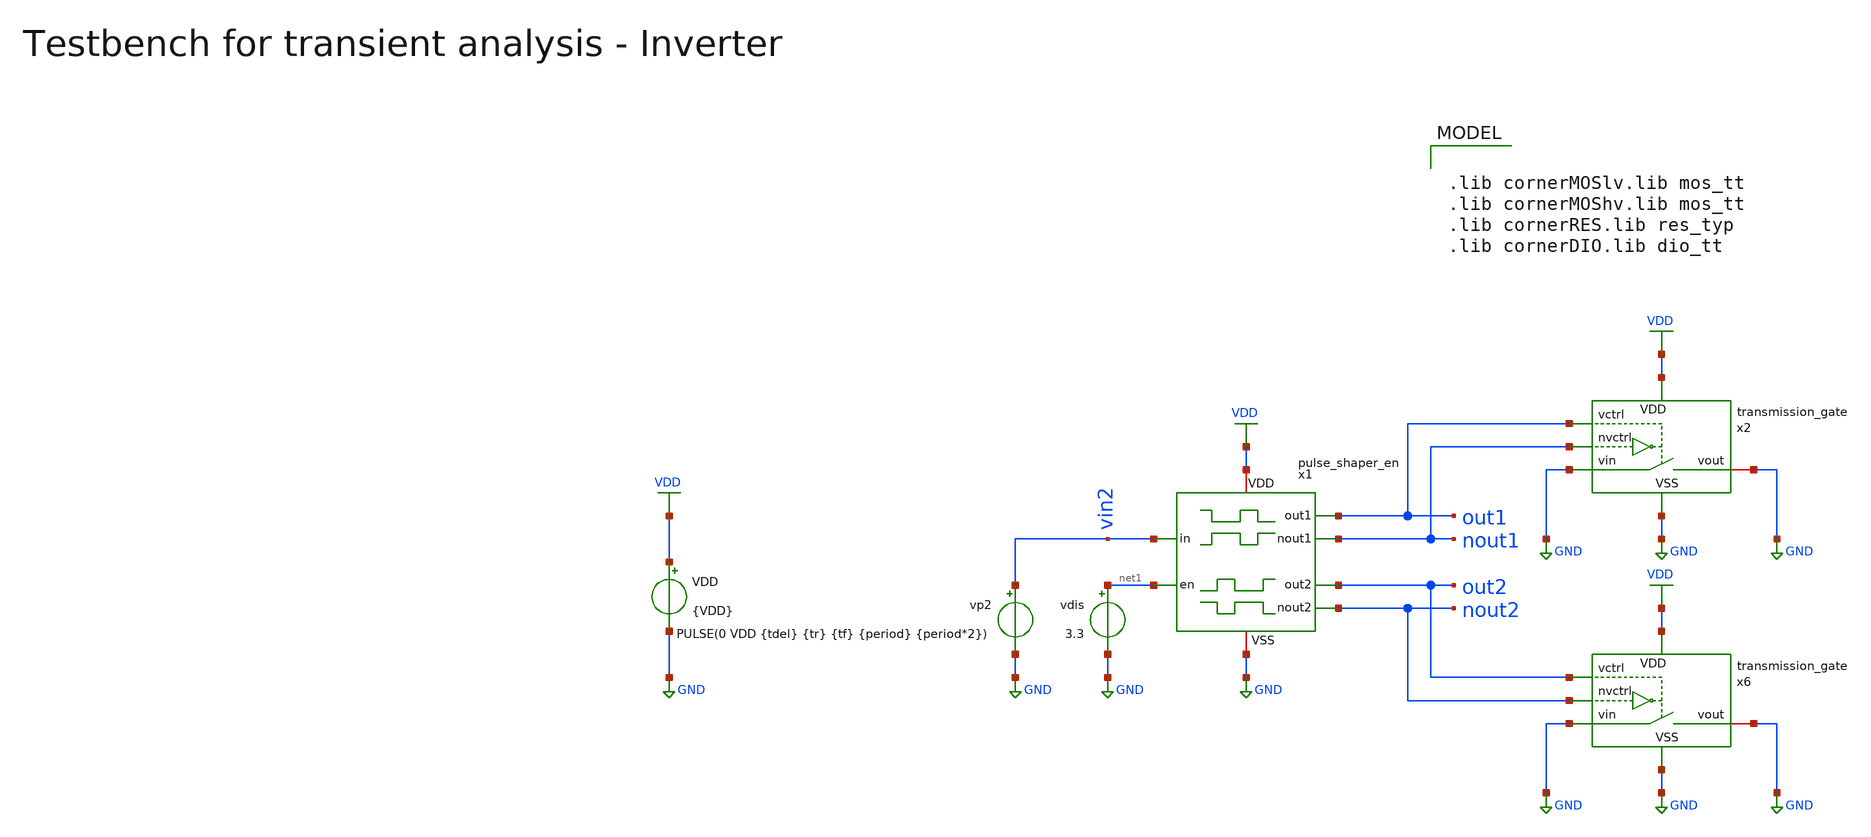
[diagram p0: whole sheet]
** sch_path: macros/heichips26_vcr/macros/switched_capacitor/testbenches/xschem/tb_pulse_shaper_en_tran.sch
**.subckt tb_pulse_shaper_en_tran
VDD VDD GND {VDD}
vp2 vin2 GND PULSE(0 VDD {tdel} {tr} {tf} {period} {period*2})
x1 out1 nout1 VDD vin2 GND out2 nout2 net1 pulse_shaper_en
vdis net1 GND 3.3
x2 out1 GND GND nout1 VDD GND transmission_gate
x6 out2 GND GND nout2 VDD GND transmission_gate
**** begin user architecture code


.param VDD=3.3
.csparam VDD=VDD
.param Vcm=VDD/2
.param temp=27
.param Cload=10p
.param Rload=1k

.param period = 4n
.param tdel   = {period/2}
.param ton    = {period*2}
.csparam tstop  = {2.5*period}
.csparam tstep  = {period/100}
.param tr     = {period/100}
.param tf     = {period/100}

.options savecurrents klu method=gear reltol=1e-4 abstol=1e-15 gmin=1e-15
.control

save all

* Transient Analysis
tran {$&tstep} {$&tstop}
write @schname\.raw

* Plotting
plot vin2
plot out1+4 out2 nout1 nout2+4


*quit
.endc



.lib cornerMOSlv.lib mos_tt
.lib cornerMOShv.lib mos_tt
.lib cornerRES.lib res_typ
.lib cornerDIO.lib dio_tt

**** end user architecture code
**.ends

* expanding   symbol:  pulse_shaper_en.sym # of pins=8
** sym_path: macros/heichips26_vcr/macros/switched_capacitor/schematic/xschem/pulse_shaper_en.sym
** sch_path: macros/heichips26_vcr/macros/switched_capacitor/schematic/xschem/pulse_shaper_en.sch
.subckt pulse_shaper_en out1 nout1 VDD in VSS out2 nout2 en
*.opin out1
*.opin nout1
*.opin out2
*.opin nout2
*.ipin in
*.iopin VSS
*.iopin VDD
*.ipin en
x7 VDD net1 net3 VSS low_th_inverter
x8 VDD net1 net2 VSS high_th_inverter
x10 VDD out1 nout1 VSS hv_inverter_40u
x11 VDD nout2 out2 VSS hv_inverter_40u
**** begin user architecture code


.include ../../../netlist/pex/hv_inverter_0u3_magic_pex_3.spice
.param w   = 0.3u
.param ng  = 1
.param n_ng = ng
.param n_w = {w*n_ng}
.param n_l = 0.45u
.param p_ng = ng
.param p_w = {1*w*p_ng}
.param p_l = 0.4u


**** end user architecture code
x1 VDD in net1 VSS hv_inverter_0u3
x5 VDD net2 out1 net4 VSS hv_nor
x4 VDD net3 nout2 en VSS hv_nand
x3 VDD en net4 VSS hv_inverter_40u
.ends


* expanding   symbol:  transmission_gate.sym # of pins=6
** sym_path: macros/heichips26_vcr/macros/switched_capacitor/schematic/xschem/transmission_gate.sym
** sch_path: macros/heichips26_vcr/macros/switched_capacitor/schematic/xschem/transmission_gate.sch
.subckt transmission_gate vctrl vin vout nvctrl VDD VSS
*.iopin vin
*.iopin vout
*.ipin vctrl
*.ipin nvctrl
*.iopin VDD
*.iopin VSS
XM3 vout vctrl vin VSS sg13_hv_nmos w={tg_ngate_w*tg_ng} l={tg_ch_len} ng={tg_ng} m=1 mm_ok=1
XM4 vout nvctrl vin VDD sg13_hv_pmos w={tg_pgate_w*tg_ng} l={tg_ch_len} ng={tg_ng} m=1 mm_ok=1
**** begin user architecture code


.param tg_ch_len=0.45u
.param tg_ngate_w=2u
.param tg_pgate_w=5u
.param tg_ng=20


**** end user architecture code
.ends


* expanding   symbol:  low_th_inverter.sym # of pins=4
** sym_path: macros/heichips26_vcr/macros/switched_capacitor/schematic/xschem/low_th_inverter.sym
** sch_path: macros/heichips26_vcr/macros/switched_capacitor/schematic/xschem/low_th_inverter.sch
.subckt low_th_inverter VDD vin vout VSS
*.ipin vin
*.iopin VDD
*.iopin VSS
*.opin vout
XM1 vout vin VSS VSS sg13_hv_nmos w={n_ng*n_w} l={n_l} ng={n_ng} m=1 mm_ok=1
XM2 vout vin VDD VDD sg13_hv_pmos w={p_ng*p_w} l={p_l} ng={n_ng} m=1 mm_ok=1
**** begin user architecture code


.param n_ng = 2
.param n_w = 1u
.param n_l = 0.45u
.param p_ng = 2
.param p_w = 1u
.param p_l = 0.4u


**** end user architecture code
.ends


* expanding   symbol:  high_th_inverter.sym # of pins=4
** sym_path: macros/heichips26_vcr/macros/switched_capacitor/schematic/xschem/high_th_inverter.sym
** sch_path: macros/heichips26_vcr/macros/switched_capacitor/schematic/xschem/high_th_inverter.sch
.subckt high_th_inverter VDD vin vout VSS
*.ipin vin
*.iopin VDD
*.iopin VSS
*.opin vout
XMdummy1 VSS VSS VSS VSS sg13_hv_nmos w=0.6u l=1.0u ng=2 m=1 mm_ok=1
XMdummy2 VDD VDD VDD VDD sg13_hv_pmos w=12.0u l=1.0u ng=2 m=1 mm_ok=1
XM1 vout vin VSS VSS sg13_hv_nmos w=6.0u l=1.0u ng=20 m=1 mm_ok=1
XM2 vout vin VDD VDD sg13_hv_pmos w=120.0u l=1.0u ng=20 m=1 mm_ok=1
.ends


* expanding   symbol:  hv_inverter_40u.sym # of pins=4
** sym_path: macros/heichips26_vcr/macros/switched_capacitor/schematic/xschem/hv_inverter_40u.sym
** sch_path: macros/heichips26_vcr/macros/switched_capacitor/schematic/xschem/hv_inverter_40u.sch
.subckt hv_inverter_40u VDD in out VSS
*.ipin in
*.iopin VDD
*.iopin VSS
*.opin out
XM2 out in VSS VSS sg13_hv_nmos w={n_w} l={n_l} ng={ng} m=1 mm_ok=1
XM3 out in VDD VDD sg13_hv_pmos w={p_w} l={p_l} ng={ng} m=1 mm_ok=1
**** begin user architecture code


.param w   = 10u
.param ng  = 4
.param n_ng = ng
.param n_w = {3u*n_ng}
.param n_l = 0.45u
.param p_ng = ng
.param p_w = {10u*p_ng}
.param p_l = 0.4u


**** end user architecture code
.ends


* expanding   symbol:  hv_inverter_0u3.sym # of pins=4
** sym_path: macros/heichips26_vcr/macros/switched_capacitor/schematic/xschem/hv_inverter_0u3.sym
** sch_path: macros/heichips26_vcr/macros/switched_capacitor/schematic/xschem/hv_inverter_0u3.sch
.subckt hv_inverter_0u3 VDD in out VSS
*.ipin in
*.iopin VDD
*.iopin VSS
*.opin out
XM2 out in VSS VSS sg13_hv_nmos w={n_w} l={n_l} ng={ng} m=1 mm_ok=1
XM3 out in VDD VDD sg13_hv_pmos w={p_w} l={p_l} ng={ng} m=1 mm_ok=1
**** begin user architecture code


.param w   = 0.3u
.param ng  = 1
.param n_ng = ng
.param n_w = {w*n_ng}
.param n_l = 0.45u
.param p_ng = ng
.param p_w = {1*w*p_ng}
.param p_l = 0.4u


**** end user architecture code
.ends


* expanding   symbol:  hv_nor.sym # of pins=5
** sym_path: macros/heichips26_vcr/macros/switched_capacitor/schematic/xschem/hv_nor.sym
** sch_path: macros/heichips26_vcr/macros/switched_capacitor/schematic/xschem/hv_nor.sch
.subckt hv_nor VDD in1 out in2 VSS
*.ipin in1
*.iopin VDD
*.iopin VSS
*.opin out
*.ipin in2
**** begin user architecture code


.param w   = 10u
.param ng  = 4
.param n_ng = ng
.param n_w = {3u*n_ng}
.param n_l = 0.45u
.param p_ng = ng
.param p_w = {10u*p_ng}
.param p_l = 0.4u


**** end user architecture code
XM2 out in1 VSS VSS sg13_hv_nmos w={n_w} l={n_l} ng={ng} m=1 mm_ok=1
XM3 net1 in2 VDD VDD sg13_hv_pmos w={p_w} l={p_l} ng={ng} m=1 mm_ok=1
XM1 out in2 VSS VSS sg13_hv_nmos w={n_w} l={n_l} ng={ng} m=1 mm_ok=1
XM4 out in1 net1 VDD sg13_hv_pmos w={p_w} l={p_l} ng={ng} m=1 mm_ok=1
.ends


* expanding   symbol:  hv_nand.sym # of pins=5
** sym_path: macros/heichips26_vcr/macros/switched_capacitor/schematic/xschem/hv_nand.sym
** sch_path: macros/heichips26_vcr/macros/switched_capacitor/schematic/xschem/hv_nand.sch
.subckt hv_nand VDD in1 out in2 VSS
*.ipin in1
*.iopin VDD
*.iopin VSS
*.opin out
*.ipin in2
**** begin user architecture code


.param w   = 10u
.param ng  = 4
.param n_ng = ng
.param n_w = {3u*n_ng}
.param n_l = 0.45u
.param p_ng = ng
.param p_w = {10u*p_ng}
.param p_l = 0.4u


**** end user architecture code
XM2 out in1 net1 VSS sg13_hv_nmos w={n_w} l={n_l} ng={ng} m=1 mm_ok=1
XM3 out in2 VDD VDD sg13_hv_pmos w={p_w} l={p_l} ng={ng} m=1 mm_ok=1
XM1 net1 in2 VSS VSS sg13_hv_nmos w={n_w} l={n_l} ng={ng} m=1 mm_ok=1
XM4 out in1 VDD VDD sg13_hv_pmos w={p_w} l={p_l} ng={ng} m=1 mm_ok=1
.ends

.GLOBAL GND
.GLOBAL VDD
.end
